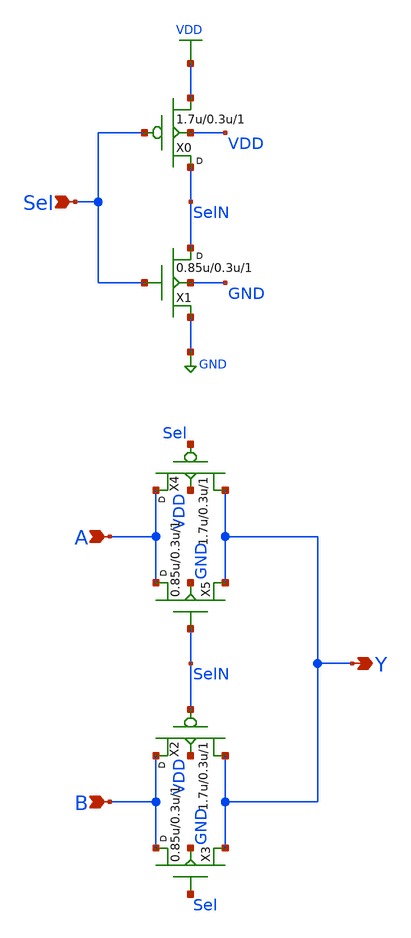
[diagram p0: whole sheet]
** sch_path: gf180mcu_osu_sc_gp9t3v3/cells/mux2/gf180mcu_osu_sc_gp9t3v3__mux2_1.sch
**.subckt gf180mcu_osu_sc_gp9t3v3__mux2_1 Sel A B Y
*.ipin Sel
*.ipin A
*.ipin B
*.opin Y
X0 SelN Sel VDD VDD pfet_03p3 w=1.7u l=0.3u m=1
X1 SelN Sel GND GND nfet_03p3 w=0.85u l=0.3u m=1
X2 B SelN Y VDD pfet_03p3 w=1.7u l=0.3u m=1
X3 B Sel Y GND nfet_03p3 w=0.85u l=0.3u m=1
X4 A Sel Y VDD pfet_03p3 w=1.7u l=0.3u m=1
X5 A SelN Y GND nfet_03p3 w=0.85u l=0.3u m=1
**.ends
.GLOBAL VDD
.GLOBAL GND
.end
